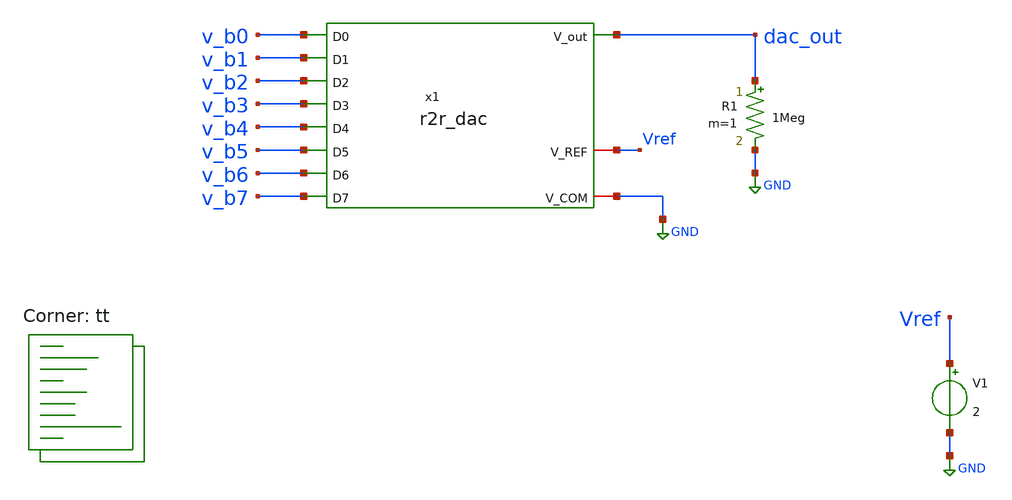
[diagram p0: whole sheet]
** sch_path: xschem/tb_dac_performance.sch
**.subckt tb_dac_performance
V1 Vref GND 2
x1 dac_out v_b7 v_b0 v_b1 v_b6 v_b2 v_b5 v_b3 v_b4 Vref GND r2r_dac
R1 dac_out GND 1Meg m=1
**** begin user architecture code
.lib $::SKYWATER_MODELS/sky130.lib.spice tt


.include "stimuli_tb_dac_codes.cir"
.param v_hi = 1.8

.control

let index = 0
let loops = 8

repeat 1
save v(dac_out) v(v_b0) v(v_b1) v(v_b2) v(v_b3) v(v_b4) v(v_b5) v(v_b6) v(v_b7)
tran 1n 1290n
write tb_dac_performance.raw
plot v(dac_out)
reset
end


*let x_ax = vector(loops)
*let v_high = vector(loops)
*let v_low = vector(loops)

*repeat $&loops
*end


.endc


**** end user architecture code
**.ends

* expanding   symbol:  r2r_dac.sym # of pins=11
** sym_path: xschem/r2r_dac.sym
** sch_path: xschem/r2r_dac.sch
.subckt r2r_dac V_out D7 D0 D1 D6 D2 D5 D3 D4 V_REF V_COM
*.ipin D0
*.opin V_out
*.iopin V_REF
*.iopin V_COM
*.ipin D1
*.ipin D2
*.ipin D3
*.ipin D7
*.ipin D6
*.ipin D5
*.ipin D4
x1 net2 net1 net3 net4 net8 net5 net7 net6 V_COM V_out R2R_20k
x2 V_REF D0 net1 V_COM dac_switch
x3 V_REF D1 net2 V_COM dac_switch
x4 V_REF D2 net3 V_COM dac_switch
x5 V_REF D3 net4 V_COM dac_switch
x6 V_REF D7 net8 V_COM dac_switch
x7 V_REF D6 net7 V_COM dac_switch
x8 V_REF D5 net6 V_COM dac_switch
x9 V_REF D4 net5 V_COM dac_switch
.ends


* expanding   symbol:  R2R_20k.sym # of pins=10
** sym_path: xschem/R2R_20k.sym
** sch_path: xschem/R2R_20k.sch
.subckt R2R_20k B1 B0 B2 B3 B7 B4 B6 B5 COM OUT
*.iopin COM
*.iopin B0
*.iopin B1
*.iopin OUT
*.iopin B2
*.iopin B3
*.iopin B4
*.iopin B5
*.iopin B6
*.iopin B7
XR1 net1 H COM sky130_fd_pr__res_xhigh_po_0p69 L=7 mult=1 m=1
XR2 B3 net1 COM sky130_fd_pr__res_xhigh_po_0p69 L=7 mult=1 m=1
XR3 net2 net13 COM sky130_fd_pr__res_xhigh_po_0p69 L=7 mult=1 m=1
XR4 B4 net2 COM sky130_fd_pr__res_xhigh_po_0p69 L=7 mult=1 m=1
XR5 net3 net14 COM sky130_fd_pr__res_xhigh_po_0p69 L=7 mult=1 m=1
XR6 B5 net3 COM sky130_fd_pr__res_xhigh_po_0p69 L=7 mult=1 m=1
XR7 net4 net15 COM sky130_fd_pr__res_xhigh_po_0p69 L=7 mult=1 m=1
XR8 B6 net4 COM sky130_fd_pr__res_xhigh_po_0p69 L=7 mult=1 m=1
XR9 net5 net9 COM sky130_fd_pr__res_xhigh_po_0p69 L=7 mult=1 m=1
XR10 COM net5 COM sky130_fd_pr__res_xhigh_po_0p69 L=7 mult=1 m=1
XR11 net6 net9 COM sky130_fd_pr__res_xhigh_po_0p69 L=7 mult=1 m=1
XR12 B0 net6 COM sky130_fd_pr__res_xhigh_po_0p69 L=7 mult=1 m=1
XR13 net7 net10 COM sky130_fd_pr__res_xhigh_po_0p69 L=7 mult=1 m=1
XR14 B1 net7 COM sky130_fd_pr__res_xhigh_po_0p69 L=7 mult=1 m=1
XR15 net8 net11 COM sky130_fd_pr__res_xhigh_po_0p69 L=7 mult=1 m=1
XR16 B2 net8 COM sky130_fd_pr__res_xhigh_po_0p69 L=7 mult=1 m=1
XR18 net10 net9 COM sky130_fd_pr__res_xhigh_po_0p69 L=7 mult=1 m=1
XR19 net11 net10 COM sky130_fd_pr__res_xhigh_po_0p69 L=7 mult=1 m=1
XR20 net13 H COM sky130_fd_pr__res_xhigh_po_0p69 L=7 mult=1 m=1
XR21 net14 net13 COM sky130_fd_pr__res_xhigh_po_0p69 L=7 mult=1 m=1
XR22 net15 net14 COM sky130_fd_pr__res_xhigh_po_0p69 L=7 mult=1 m=1
XR17 net12 OUT COM sky130_fd_pr__res_xhigh_po_0p69 L=7 mult=1 m=1
XR23 B7 net12 COM sky130_fd_pr__res_xhigh_po_0p69 L=7 mult=1 m=1
XR24 OUT net15 COM sky130_fd_pr__res_xhigh_po_0p69 L=7 mult=1 m=1
XR25 H net11 COM sky130_fd_pr__res_xhigh_po_0p69 L=7 mult=1 m=1
.ends


* expanding   symbol:  dac_switch.sym # of pins=4
** sym_path: xschem/dac_switch.sym
** sch_path: xschem/dac_switch.sch
.subckt dac_switch Vref Dx Outx Vcom
*.ipin Dx
*.opin Outx
*.iopin Vref
*.iopin Vcom
XM1 Outx Dx Vref Vref sky130_fd_pr__pfet_g5v0d10v5 L=0.5 W=16 nf=1 ad='int((nf+1)/2) * W/nf * 0.29' as='int((nf+2)/2) * W/nf * 0.29'
+ pd='2*int((nf+1)/2) * (W/nf + 0.29)' ps='2*int((nf+2)/2) * (W/nf + 0.29)' nrd='0.29 / W' nrs='0.29 / W'
+ sa=0 sb=0 sd=0 mult=1 m=1
XM2 Outx Dx Vcom Vcom sky130_fd_pr__nfet_g5v0d10v5 L=0.5 W=7 nf=1 ad='int((nf+1)/2) * W/nf * 0.29' as='int((nf+2)/2) * W/nf * 0.29'
+ pd='2*int((nf+1)/2) * (W/nf + 0.29)' ps='2*int((nf+2)/2) * (W/nf + 0.29)' nrd='0.29 / W' nrs='0.29 / W'
+ sa=0 sb=0 sd=0 mult=1 m=1
.ends

.GLOBAL GND
.end
